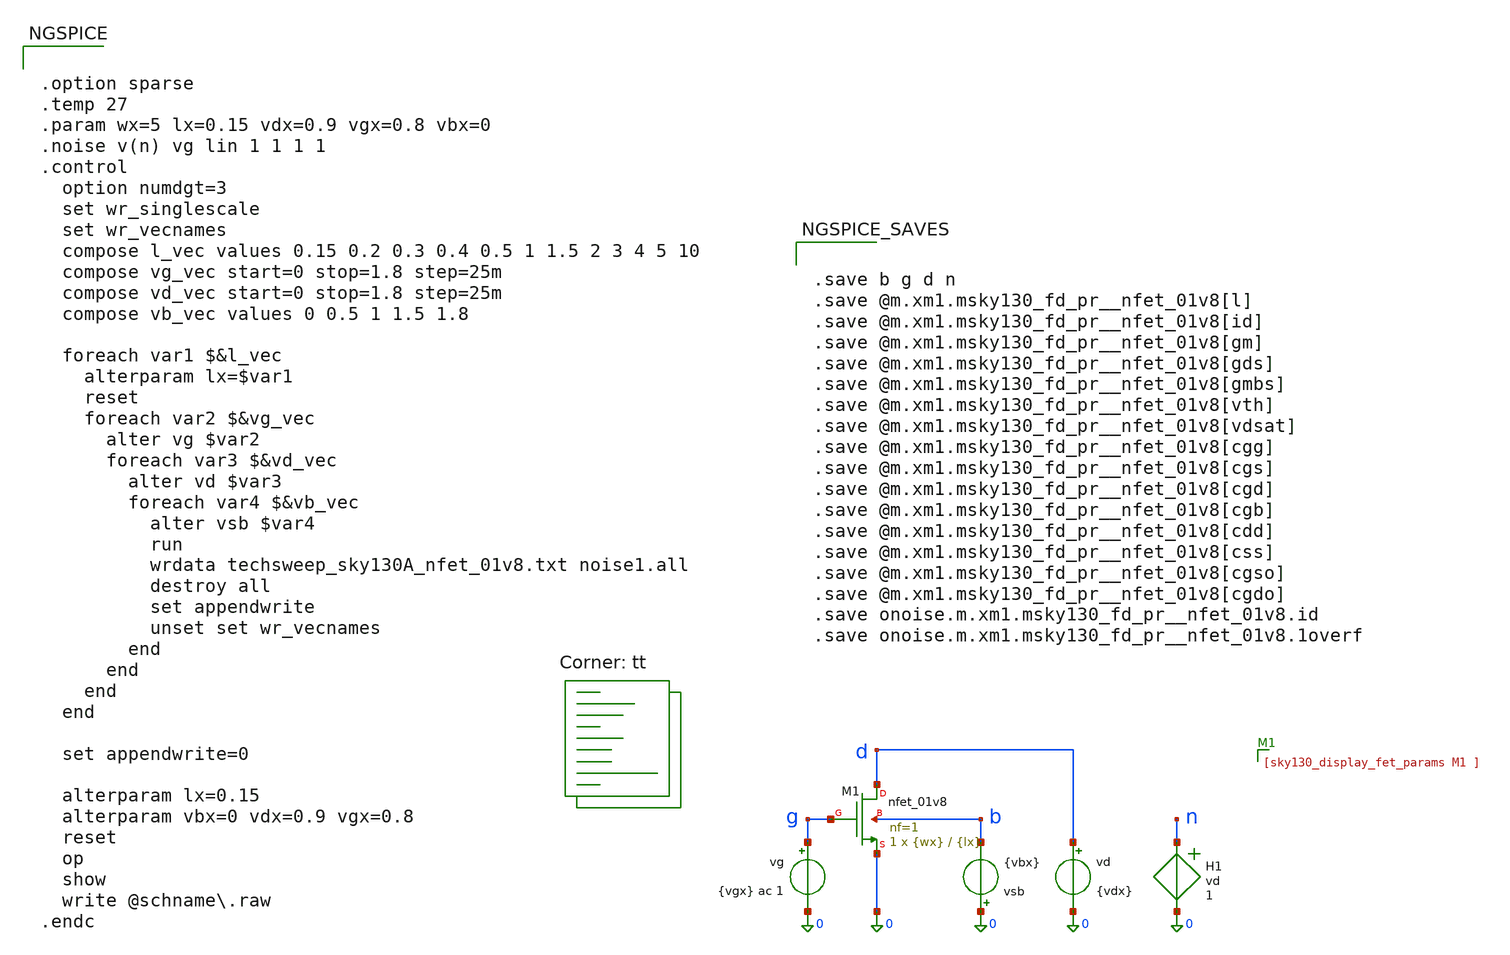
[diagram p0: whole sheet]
** sch_path: sch/gmid/gmid_nmos.sch
**.subckt gmid_nmos
XM1 d g 0 b sky130_fd_pr__nfet_01v8 L={lx} W={wx} nf=1 ad='int((1 + 1)/2) * {wx} / 1 * 0.29' as='int((1 + 2)/2) * {wx} / 1 * 0.29'
+ pd='2*int((1 + 1)/2) * ({wx} / 1 + 0.29)' ps='2*int((1 + 2)/2) * ({wx} / 1 + 0.29)' nrd='0.29 / {wx} '
+ nrs='0.29 / {wx} ' sa=0 sb=0 sd=0 mult=1 m=1
vsb 0 b {vbx}
vd d 0 {vdx}
vg g 0 {vgx} ac 1
H1 n 0 vd 1
**** begin user architecture code
.lib $::SKYWATER_MODELS/sky130.lib.spice tt


.option sparse
.temp 27
.param wx=5 lx=0.15 vdx=0.9 vgx=0.8 vbx=0
.noise v(n) vg lin 1 1 1 1
.control
  option numdgt=3
  set wr_singlescale
  set wr_vecnames
  compose l_vec values 0.15 0.2 0.3 0.4 0.5 1 1.5 2 3 4 5 10
  compose vg_vec start=0 stop=1.8 step=25m
  compose vd_vec start=0 stop=1.8 step=25m
  compose vb_vec values 0 0.5 1 1.5 1.8

  foreach var1 $&l_vec
    alterparam lx=$var1
    reset
    foreach var2 $&vg_vec
      alter vg $var2
      foreach var3 $&vd_vec
        alter vd $var3
        foreach var4 $&vb_vec
          alter vsb $var4
          run
          wrdata techsweep_sky130A_nfet_01v8.txt noise1.all
          destroy all
          set appendwrite
          unset set wr_vecnames
        end
      end
    end
  end

  set appendwrite=0

  alterparam lx=0.15
  alterparam vbx=0 vdx=0.9 vgx=0.8
  reset
  op
  show
  write @schname\.raw
.endc




.save b g d n
.save @m.xm1.msky130_fd_pr__nfet_01v8[l]
.save @m.xm1.msky130_fd_pr__nfet_01v8[id]
.save @m.xm1.msky130_fd_pr__nfet_01v8[gm]
.save @m.xm1.msky130_fd_pr__nfet_01v8[gds]
.save @m.xm1.msky130_fd_pr__nfet_01v8[gmbs]
.save @m.xm1.msky130_fd_pr__nfet_01v8[vth]
.save @m.xm1.msky130_fd_pr__nfet_01v8[vdsat]
.save @m.xm1.msky130_fd_pr__nfet_01v8[cgg]
.save @m.xm1.msky130_fd_pr__nfet_01v8[cgs]
.save @m.xm1.msky130_fd_pr__nfet_01v8[cgd]
.save @m.xm1.msky130_fd_pr__nfet_01v8[cgb]
.save @m.xm1.msky130_fd_pr__nfet_01v8[cdd]
.save @m.xm1.msky130_fd_pr__nfet_01v8[css]
.save @m.xm1.msky130_fd_pr__nfet_01v8[cgso]
.save @m.xm1.msky130_fd_pr__nfet_01v8[cgdo]
.save onoise.m.xm1.msky130_fd_pr__nfet_01v8.id
.save onoise.m.xm1.msky130_fd_pr__nfet_01v8.1overf


**** end user architecture code
**.ends
.end
